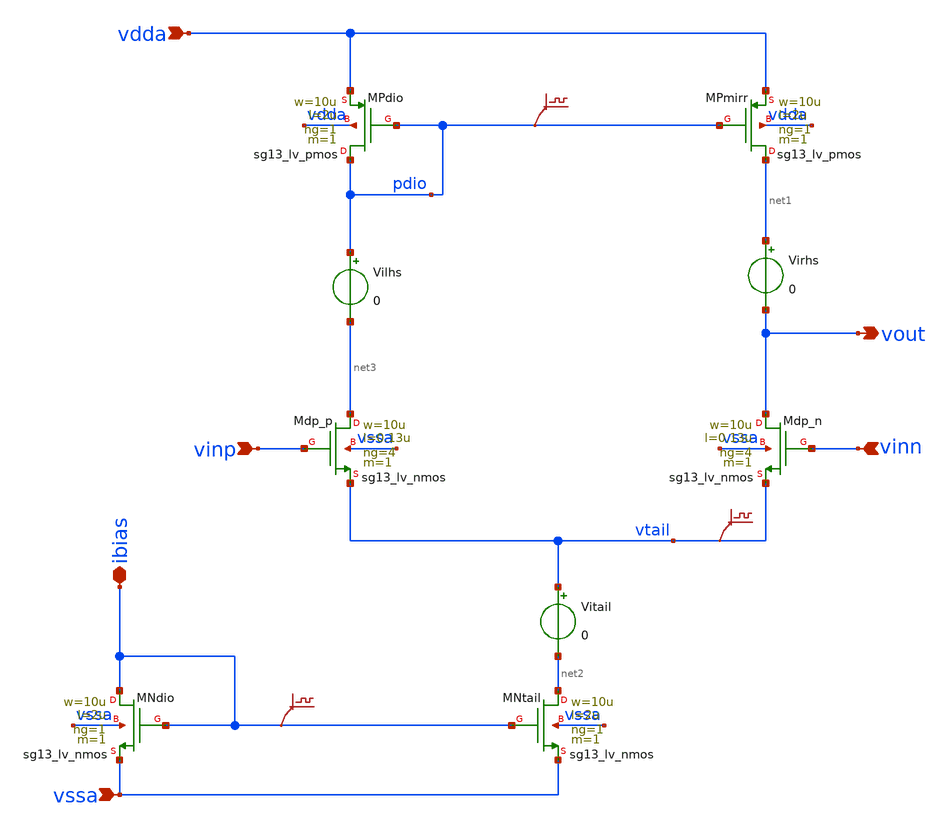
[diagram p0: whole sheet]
** sch_path: tb_OTA_1stage_ihp/OTA_DCOP.sch
**.subckt OTA_DCOP ibias vdda vssa vinp vinn vout
*.iopin ibias
*.ipin vdda
*.ipin vssa
*.ipin vinp
*.ipin vinn
*.opin vout
XMPmirr net1 pdio vdda vdda sg13_lv_pmos w=10u l=2u ng=1 m=1 mm_ok=1
XMdp_p net3 vinp vtail vssa sg13_lv_nmos w=10u l=0.13u ng=4 m=1 mm_ok=1
XMPdio pdio pdio vdda vdda sg13_lv_pmos w=10u l=2u ng=1 m=1 mm_ok=1
XMdp_n vout vinn vtail vssa sg13_lv_nmos w=10u l=0.13u ng=4 m=1 mm_ok=1
XMNtail net2 ibias vssa vssa sg13_lv_nmos w=10u l=2u ng=1 m=1 mm_ok=1
XMNdio ibias ibias vssa vssa sg13_lv_nmos w=10u l=2u ng=1 m=1 mm_ok=1
.save v(vtail)
.save v(pdio)
.save v(ibias)
Vitail vtail net2 0
Virhs net1 vout 0
Vilhs pdio net3 0
**.ends
.end
